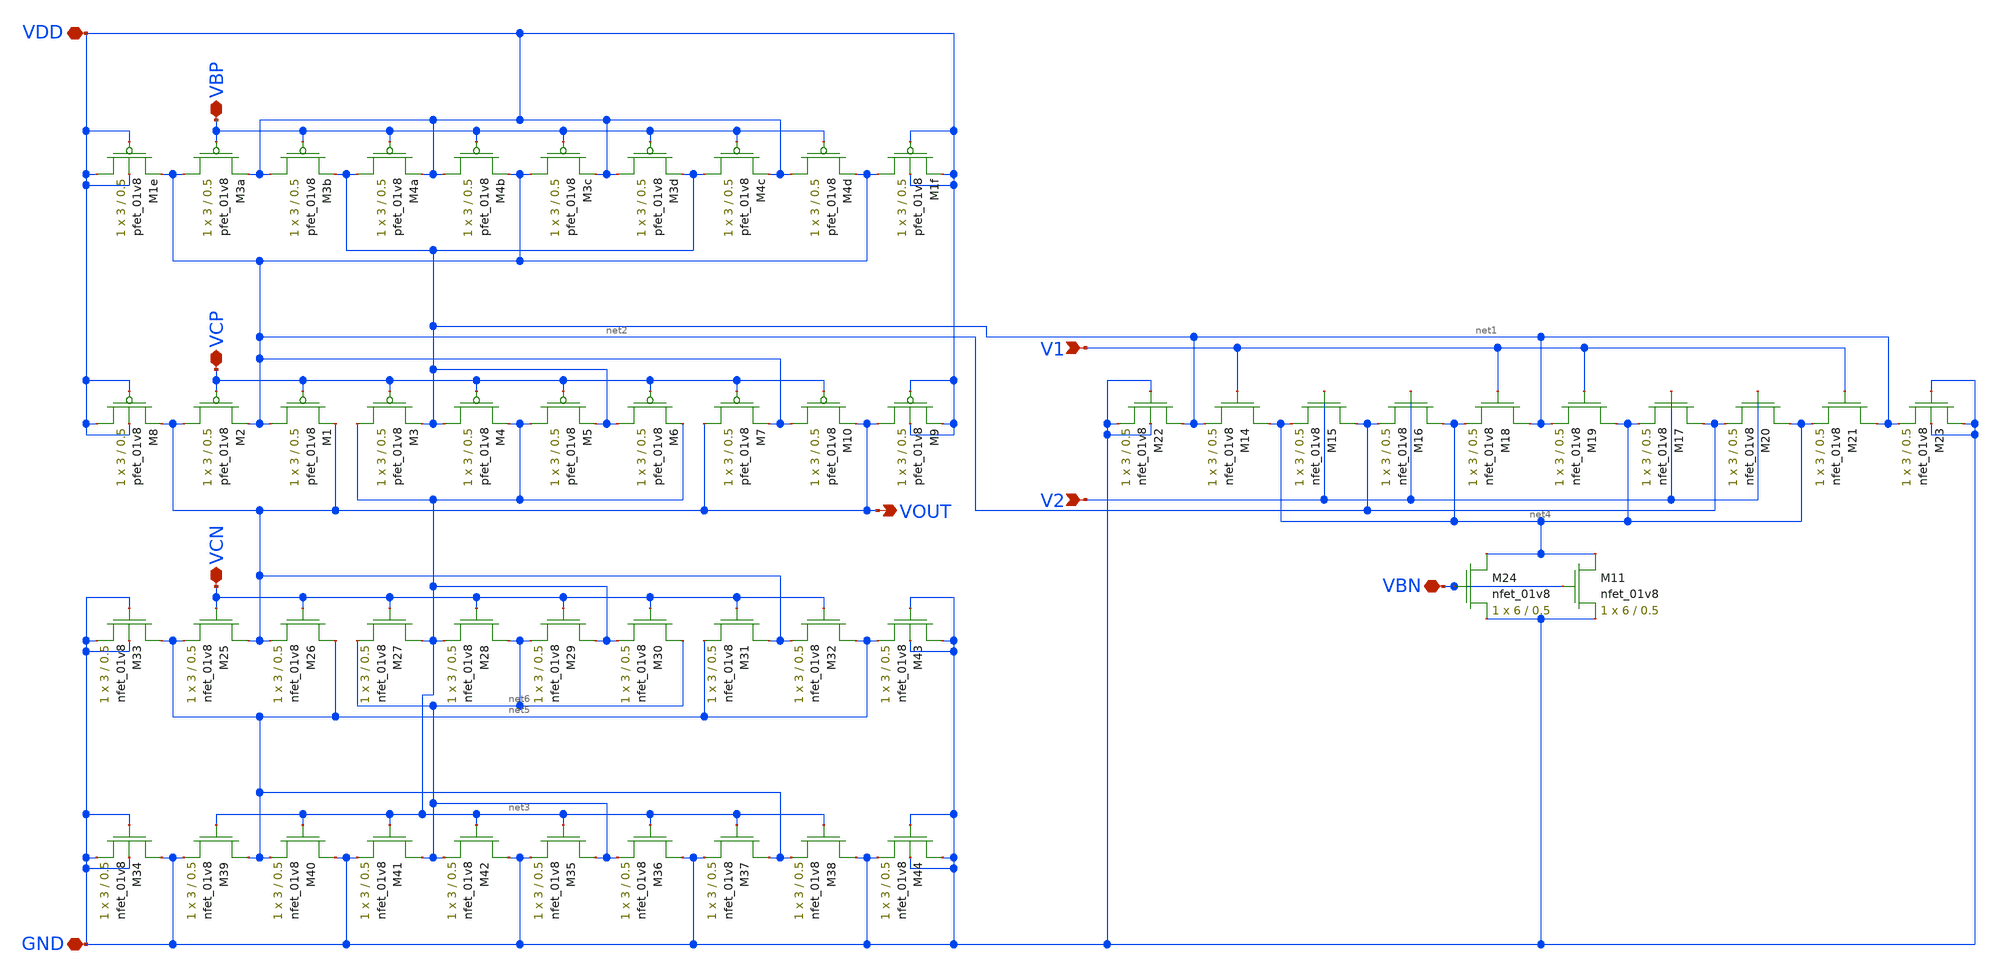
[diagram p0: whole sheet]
** sch_path: mp3/schematics/differential_amplifier.sch
**.subckt differential_amplifier VBP VCP V1 V2 VBN VCN VDD GND VOUT
*.iopin VBP
*.iopin VCP
*.ipin V1
*.ipin V2
*.iopin VBN
*.iopin VCN
*.iopin VDD
*.iopin GND
*.opin VOUT
XM3b VDD VBP net1 VDD sky130_fd_pr__pfet_01v8 L=0.5 W=3 nf=1 ad='int((nf+1)/2) * W/nf * 0.29' as='int((nf+2)/2) * W/nf * 0.29'
+ pd='2*int((nf+1)/2) * (W/nf + 0.29)' ps='2*int((nf+2)/2) * (W/nf + 0.29)' nrd='0.29 / W' nrs='0.29 / W'
+ sa=0 sb=0 sd=0 mult=1 m=1
XM3a net2 VBP VDD VDD sky130_fd_pr__pfet_01v8 L=0.5 W=3 nf=1 ad='int((nf+1)/2) * W/nf * 0.29' as='int((nf+2)/2) * W/nf * 0.29'
+ pd='2*int((nf+1)/2) * (W/nf + 0.29)' ps='2*int((nf+2)/2) * (W/nf + 0.29)' nrd='0.29 / W' nrs='0.29 / W'
+ sa=0 sb=0 sd=0 mult=1 m=1
XM4a net1 VBP VDD VDD sky130_fd_pr__pfet_01v8 L=0.5 W=3 nf=1 ad='int((nf+1)/2) * W/nf * 0.29' as='int((nf+2)/2) * W/nf * 0.29'
+ pd='2*int((nf+1)/2) * (W/nf + 0.29)' ps='2*int((nf+2)/2) * (W/nf + 0.29)' nrd='0.29 / W' nrs='0.29 / W'
+ sa=0 sb=0 sd=0 mult=1 m=1
XM4b VDD VBP net2 VDD sky130_fd_pr__pfet_01v8 L=0.5 W=3 nf=1 ad='int((nf+1)/2) * W/nf * 0.29' as='int((nf+2)/2) * W/nf * 0.29'
+ pd='2*int((nf+1)/2) * (W/nf + 0.29)' ps='2*int((nf+2)/2) * (W/nf + 0.29)' nrd='0.29 / W' nrs='0.29 / W'
+ sa=0 sb=0 sd=0 mult=1 m=1
XM3c net2 VBP VDD VDD sky130_fd_pr__pfet_01v8 L=0.5 W=3 nf=1 ad='int((nf+1)/2) * W/nf * 0.29' as='int((nf+2)/2) * W/nf * 0.29'
+ pd='2*int((nf+1)/2) * (W/nf + 0.29)' ps='2*int((nf+2)/2) * (W/nf + 0.29)' nrd='0.29 / W' nrs='0.29 / W'
+ sa=0 sb=0 sd=0 mult=1 m=1
XM3d VDD VBP net1 VDD sky130_fd_pr__pfet_01v8 L=0.5 W=3 nf=1 ad='int((nf+1)/2) * W/nf * 0.29' as='int((nf+2)/2) * W/nf * 0.29'
+ pd='2*int((nf+1)/2) * (W/nf + 0.29)' ps='2*int((nf+2)/2) * (W/nf + 0.29)' nrd='0.29 / W' nrs='0.29 / W'
+ sa=0 sb=0 sd=0 mult=1 m=1
XM4c net1 VBP VDD VDD sky130_fd_pr__pfet_01v8 L=0.5 W=3 nf=1 ad='int((nf+1)/2) * W/nf * 0.29' as='int((nf+2)/2) * W/nf * 0.29'
+ pd='2*int((nf+1)/2) * (W/nf + 0.29)' ps='2*int((nf+2)/2) * (W/nf + 0.29)' nrd='0.29 / W' nrs='0.29 / W'
+ sa=0 sb=0 sd=0 mult=1 m=1
XM1e VDD VDD net2 VDD sky130_fd_pr__pfet_01v8 L=0.5 W=3 nf=1 ad='int((nf+1)/2) * W/nf * 0.29' as='int((nf+2)/2) * W/nf * 0.29'
+ pd='2*int((nf+1)/2) * (W/nf + 0.29)' ps='2*int((nf+2)/2) * (W/nf + 0.29)' nrd='0.29 / W' nrs='0.29 / W'
+ sa=0 sb=0 sd=0 mult=1 m=1
XM1f net2 VDD VDD VDD sky130_fd_pr__pfet_01v8 L=0.5 W=3 nf=1 ad='int((nf+1)/2) * W/nf * 0.29' as='int((nf+2)/2) * W/nf * 0.29'
+ pd='2*int((nf+1)/2) * (W/nf + 0.29)' ps='2*int((nf+2)/2) * (W/nf + 0.29)' nrd='0.29 / W' nrs='0.29 / W'
+ sa=0 sb=0 sd=0 mult=1 m=1
XM4d VDD VBP net2 VDD sky130_fd_pr__pfet_01v8 L=0.5 W=3 nf=1 ad='int((nf+1)/2) * W/nf * 0.29' as='int((nf+2)/2) * W/nf * 0.29'
+ pd='2*int((nf+1)/2) * (W/nf + 0.29)' ps='2*int((nf+2)/2) * (W/nf + 0.29)' nrd='0.29 / W' nrs='0.29 / W'
+ sa=0 sb=0 sd=0 mult=1 m=1
XM1 net2 VCP VOUT VDD sky130_fd_pr__pfet_01v8 L=0.5 W=3 nf=1 ad='int((nf+1)/2) * W/nf * 0.29' as='int((nf+2)/2) * W/nf * 0.29'
+ pd='2*int((nf+1)/2) * (W/nf + 0.29)' ps='2*int((nf+2)/2) * (W/nf + 0.29)' nrd='0.29 / W' nrs='0.29 / W'
+ sa=0 sb=0 sd=0 mult=1 m=1
XM2 VOUT VCP net2 VDD sky130_fd_pr__pfet_01v8 L=0.5 W=3 nf=1 ad='int((nf+1)/2) * W/nf * 0.29' as='int((nf+2)/2) * W/nf * 0.29'
+ pd='2*int((nf+1)/2) * (W/nf + 0.29)' ps='2*int((nf+2)/2) * (W/nf + 0.29)' nrd='0.29 / W' nrs='0.29 / W'
+ sa=0 sb=0 sd=0 mult=1 m=1
XM3 net3 VCP net1 VDD sky130_fd_pr__pfet_01v8 L=0.5 W=3 nf=1 ad='int((nf+1)/2) * W/nf * 0.29' as='int((nf+2)/2) * W/nf * 0.29'
+ pd='2*int((nf+1)/2) * (W/nf + 0.29)' ps='2*int((nf+2)/2) * (W/nf + 0.29)' nrd='0.29 / W' nrs='0.29 / W'
+ sa=0 sb=0 sd=0 mult=1 m=1
XM4 net1 VCP net3 VDD sky130_fd_pr__pfet_01v8 L=0.5 W=3 nf=1 ad='int((nf+1)/2) * W/nf * 0.29' as='int((nf+2)/2) * W/nf * 0.29'
+ pd='2*int((nf+1)/2) * (W/nf + 0.29)' ps='2*int((nf+2)/2) * (W/nf + 0.29)' nrd='0.29 / W' nrs='0.29 / W'
+ sa=0 sb=0 sd=0 mult=1 m=1
XM5 net3 VCP net1 VDD sky130_fd_pr__pfet_01v8 L=0.5 W=3 nf=1 ad='int((nf+1)/2) * W/nf * 0.29' as='int((nf+2)/2) * W/nf * 0.29'
+ pd='2*int((nf+1)/2) * (W/nf + 0.29)' ps='2*int((nf+2)/2) * (W/nf + 0.29)' nrd='0.29 / W' nrs='0.29 / W'
+ sa=0 sb=0 sd=0 mult=1 m=1
XM6 net1 VCP net3 VDD sky130_fd_pr__pfet_01v8 L=0.5 W=3 nf=1 ad='int((nf+1)/2) * W/nf * 0.29' as='int((nf+2)/2) * W/nf * 0.29'
+ pd='2*int((nf+1)/2) * (W/nf + 0.29)' ps='2*int((nf+2)/2) * (W/nf + 0.29)' nrd='0.29 / W' nrs='0.29 / W'
+ sa=0 sb=0 sd=0 mult=1 m=1
XM7 VOUT VCP net2 VDD sky130_fd_pr__pfet_01v8 L=0.5 W=3 nf=1 ad='int((nf+1)/2) * W/nf * 0.29' as='int((nf+2)/2) * W/nf * 0.29'
+ pd='2*int((nf+1)/2) * (W/nf + 0.29)' ps='2*int((nf+2)/2) * (W/nf + 0.29)' nrd='0.29 / W' nrs='0.29 / W'
+ sa=0 sb=0 sd=0 mult=1 m=1
XM8 VDD VDD VOUT VDD sky130_fd_pr__pfet_01v8 L=0.5 W=3 nf=1 ad='int((nf+1)/2) * W/nf * 0.29' as='int((nf+2)/2) * W/nf * 0.29'
+ pd='2*int((nf+1)/2) * (W/nf + 0.29)' ps='2*int((nf+2)/2) * (W/nf + 0.29)' nrd='0.29 / W' nrs='0.29 / W'
+ sa=0 sb=0 sd=0 mult=1 m=1
XM9 VOUT VDD VDD VDD sky130_fd_pr__pfet_01v8 L=0.5 W=3 nf=1 ad='int((nf+1)/2) * W/nf * 0.29' as='int((nf+2)/2) * W/nf * 0.29'
+ pd='2*int((nf+1)/2) * (W/nf + 0.29)' ps='2*int((nf+2)/2) * (W/nf + 0.29)' nrd='0.29 / W' nrs='0.29 / W'
+ sa=0 sb=0 sd=0 mult=1 m=1
XM10 net2 VCP VOUT VDD sky130_fd_pr__pfet_01v8 L=0.5 W=3 nf=1 ad='int((nf+1)/2) * W/nf * 0.29' as='int((nf+2)/2) * W/nf * 0.29'
+ pd='2*int((nf+1)/2) * (W/nf + 0.29)' ps='2*int((nf+2)/2) * (W/nf + 0.29)' nrd='0.29 / W' nrs='0.29 / W'
+ sa=0 sb=0 sd=0 mult=1 m=1
XM14 net4 V1 net1 GND sky130_fd_pr__nfet_01v8 L=0.5 W=3 nf=1 ad='int((nf+1)/2) * W/nf * 0.29' as='int((nf+2)/2) * W/nf * 0.29'
+ pd='2*int((nf+1)/2) * (W/nf + 0.29)' ps='2*int((nf+2)/2) * (W/nf + 0.29)' nrd='0.29 / W' nrs='0.29 / W'
+ sa=0 sb=0 sd=0 mult=1 m=1
XM22 net1 GND GND GND sky130_fd_pr__nfet_01v8 L=0.5 W=3 nf=1 ad='int((nf+1)/2) * W/nf * 0.29' as='int((nf+2)/2) * W/nf * 0.29'
+ pd='2*int((nf+1)/2) * (W/nf + 0.29)' ps='2*int((nf+2)/2) * (W/nf + 0.29)' nrd='0.29 / W' nrs='0.29 / W'
+ sa=0 sb=0 sd=0 mult=1 m=1
XM23 GND GND net1 GND sky130_fd_pr__nfet_01v8 L=0.5 W=3 nf=1 ad='int((nf+1)/2) * W/nf * 0.29' as='int((nf+2)/2) * W/nf * 0.29'
+ pd='2*int((nf+1)/2) * (W/nf + 0.29)' ps='2*int((nf+2)/2) * (W/nf + 0.29)' nrd='0.29 / W' nrs='0.29 / W'
+ sa=0 sb=0 sd=0 mult=1 m=1
XM15 net2 V2 net4 GND sky130_fd_pr__nfet_01v8 L=0.5 W=3 nf=1 ad='int((nf+1)/2) * W/nf * 0.29' as='int((nf+2)/2) * W/nf * 0.29'
+ pd='2*int((nf+1)/2) * (W/nf + 0.29)' ps='2*int((nf+2)/2) * (W/nf + 0.29)' nrd='0.29 / W' nrs='0.29 / W'
+ sa=0 sb=0 sd=0 mult=1 m=1
XM16 net4 V2 net2 GND sky130_fd_pr__nfet_01v8 L=0.5 W=3 nf=1 ad='int((nf+1)/2) * W/nf * 0.29' as='int((nf+2)/2) * W/nf * 0.29'
+ pd='2*int((nf+1)/2) * (W/nf + 0.29)' ps='2*int((nf+2)/2) * (W/nf + 0.29)' nrd='0.29 / W' nrs='0.29 / W'
+ sa=0 sb=0 sd=0 mult=1 m=1
XM17 net2 V2 net4 GND sky130_fd_pr__nfet_01v8 L=0.5 W=3 nf=1 ad='int((nf+1)/2) * W/nf * 0.29' as='int((nf+2)/2) * W/nf * 0.29'
+ pd='2*int((nf+1)/2) * (W/nf + 0.29)' ps='2*int((nf+2)/2) * (W/nf + 0.29)' nrd='0.29 / W' nrs='0.29 / W'
+ sa=0 sb=0 sd=0 mult=1 m=1
XM18 net1 V1 net4 GND sky130_fd_pr__nfet_01v8 L=0.5 W=3 nf=1 ad='int((nf+1)/2) * W/nf * 0.29' as='int((nf+2)/2) * W/nf * 0.29'
+ pd='2*int((nf+1)/2) * (W/nf + 0.29)' ps='2*int((nf+2)/2) * (W/nf + 0.29)' nrd='0.29 / W' nrs='0.29 / W'
+ sa=0 sb=0 sd=0 mult=1 m=1
XM19 net4 V1 net1 GND sky130_fd_pr__nfet_01v8 L=0.5 W=3 nf=1 ad='int((nf+1)/2) * W/nf * 0.29' as='int((nf+2)/2) * W/nf * 0.29'
+ pd='2*int((nf+1)/2) * (W/nf + 0.29)' ps='2*int((nf+2)/2) * (W/nf + 0.29)' nrd='0.29 / W' nrs='0.29 / W'
+ sa=0 sb=0 sd=0 mult=1 m=1
XM20 net4 V2 net2 GND sky130_fd_pr__nfet_01v8 L=0.5 W=3 nf=1 ad='int((nf+1)/2) * W/nf * 0.29' as='int((nf+2)/2) * W/nf * 0.29'
+ pd='2*int((nf+1)/2) * (W/nf + 0.29)' ps='2*int((nf+2)/2) * (W/nf + 0.29)' nrd='0.29 / W' nrs='0.29 / W'
+ sa=0 sb=0 sd=0 mult=1 m=1
XM21 net1 V1 net4 GND sky130_fd_pr__nfet_01v8 L=0.5 W=3 nf=1 ad='int((nf+1)/2) * W/nf * 0.29' as='int((nf+2)/2) * W/nf * 0.29'
+ pd='2*int((nf+1)/2) * (W/nf + 0.29)' ps='2*int((nf+2)/2) * (W/nf + 0.29)' nrd='0.29 / W' nrs='0.29 / W'
+ sa=0 sb=0 sd=0 mult=1 m=1
XM24 net4 VBN GND GND sky130_fd_pr__nfet_01v8 L=0.5 W=6 nf=1 ad='int((nf+1)/2) * W/nf * 0.29' as='int((nf+2)/2) * W/nf * 0.29'
+ pd='2*int((nf+1)/2) * (W/nf + 0.29)' ps='2*int((nf+2)/2) * (W/nf + 0.29)' nrd='0.29 / W' nrs='0.29 / W'
+ sa=0 sb=0 sd=0 mult=1 m=1
XM29 net3 VCN net6 GND sky130_fd_pr__nfet_01v8 L=0.5 W=3 nf=1 ad='int((nf+1)/2) * W/nf * 0.29' as='int((nf+2)/2) * W/nf * 0.29'
+ pd='2*int((nf+1)/2) * (W/nf + 0.29)' ps='2*int((nf+2)/2) * (W/nf + 0.29)' nrd='0.29 / W' nrs='0.29 / W'
+ sa=0 sb=0 sd=0 mult=1 m=1
XM30 net6 VCN net3 GND sky130_fd_pr__nfet_01v8 L=0.5 W=3 nf=1 ad='int((nf+1)/2) * W/nf * 0.29' as='int((nf+2)/2) * W/nf * 0.29'
+ pd='2*int((nf+1)/2) * (W/nf + 0.29)' ps='2*int((nf+2)/2) * (W/nf + 0.29)' nrd='0.29 / W' nrs='0.29 / W'
+ sa=0 sb=0 sd=0 mult=1 m=1
XM31 VOUT VCN net5 GND sky130_fd_pr__nfet_01v8 L=0.5 W=3 nf=1 ad='int((nf+1)/2) * W/nf * 0.29' as='int((nf+2)/2) * W/nf * 0.29'
+ pd='2*int((nf+1)/2) * (W/nf + 0.29)' ps='2*int((nf+2)/2) * (W/nf + 0.29)' nrd='0.29 / W' nrs='0.29 / W'
+ sa=0 sb=0 sd=0 mult=1 m=1
XM32 net5 VCN VOUT GND sky130_fd_pr__nfet_01v8 L=0.5 W=3 nf=1 ad='int((nf+1)/2) * W/nf * 0.29' as='int((nf+2)/2) * W/nf * 0.29'
+ pd='2*int((nf+1)/2) * (W/nf + 0.29)' ps='2*int((nf+2)/2) * (W/nf + 0.29)' nrd='0.29 / W' nrs='0.29 / W'
+ sa=0 sb=0 sd=0 mult=1 m=1
XM25 VOUT VCN net5 GND sky130_fd_pr__nfet_01v8 L=0.5 W=3 nf=1 ad='int((nf+1)/2) * W/nf * 0.29' as='int((nf+2)/2) * W/nf * 0.29'
+ pd='2*int((nf+1)/2) * (W/nf + 0.29)' ps='2*int((nf+2)/2) * (W/nf + 0.29)' nrd='0.29 / W' nrs='0.29 / W'
+ sa=0 sb=0 sd=0 mult=1 m=1
XM26 net5 VCN VOUT GND sky130_fd_pr__nfet_01v8 L=0.5 W=3 nf=1 ad='int((nf+1)/2) * W/nf * 0.29' as='int((nf+2)/2) * W/nf * 0.29'
+ pd='2*int((nf+1)/2) * (W/nf + 0.29)' ps='2*int((nf+2)/2) * (W/nf + 0.29)' nrd='0.29 / W' nrs='0.29 / W'
+ sa=0 sb=0 sd=0 mult=1 m=1
XM27 net3 VCN net6 GND sky130_fd_pr__nfet_01v8 L=0.5 W=3 nf=1 ad='int((nf+1)/2) * W/nf * 0.29' as='int((nf+2)/2) * W/nf * 0.29'
+ pd='2*int((nf+1)/2) * (W/nf + 0.29)' ps='2*int((nf+2)/2) * (W/nf + 0.29)' nrd='0.29 / W' nrs='0.29 / W'
+ sa=0 sb=0 sd=0 mult=1 m=1
XM28 net6 VCN net3 GND sky130_fd_pr__nfet_01v8 L=0.5 W=3 nf=1 ad='int((nf+1)/2) * W/nf * 0.29' as='int((nf+2)/2) * W/nf * 0.29'
+ pd='2*int((nf+1)/2) * (W/nf + 0.29)' ps='2*int((nf+2)/2) * (W/nf + 0.29)' nrd='0.29 / W' nrs='0.29 / W'
+ sa=0 sb=0 sd=0 mult=1 m=1
XM35 net6 net3 GND GND sky130_fd_pr__nfet_01v8 L=0.5 W=3 nf=1 ad='int((nf+1)/2) * W/nf * 0.29' as='int((nf+2)/2) * W/nf * 0.29'
+ pd='2*int((nf+1)/2) * (W/nf + 0.29)' ps='2*int((nf+2)/2) * (W/nf + 0.29)' nrd='0.29 / W' nrs='0.29 / W'
+ sa=0 sb=0 sd=0 mult=1 m=1
XM36 GND net3 net6 GND sky130_fd_pr__nfet_01v8 L=0.5 W=3 nf=1 ad='int((nf+1)/2) * W/nf * 0.29' as='int((nf+2)/2) * W/nf * 0.29'
+ pd='2*int((nf+1)/2) * (W/nf + 0.29)' ps='2*int((nf+2)/2) * (W/nf + 0.29)' nrd='0.29 / W' nrs='0.29 / W'
+ sa=0 sb=0 sd=0 mult=1 m=1
XM37 net5 net3 GND GND sky130_fd_pr__nfet_01v8 L=0.5 W=3 nf=1 ad='int((nf+1)/2) * W/nf * 0.29' as='int((nf+2)/2) * W/nf * 0.29'
+ pd='2*int((nf+1)/2) * (W/nf + 0.29)' ps='2*int((nf+2)/2) * (W/nf + 0.29)' nrd='0.29 / W' nrs='0.29 / W'
+ sa=0 sb=0 sd=0 mult=1 m=1
XM38 GND net3 net5 GND sky130_fd_pr__nfet_01v8 L=0.5 W=3 nf=1 ad='int((nf+1)/2) * W/nf * 0.29' as='int((nf+2)/2) * W/nf * 0.29'
+ pd='2*int((nf+1)/2) * (W/nf + 0.29)' ps='2*int((nf+2)/2) * (W/nf + 0.29)' nrd='0.29 / W' nrs='0.29 / W'
+ sa=0 sb=0 sd=0 mult=1 m=1
XM39 net5 net3 GND GND sky130_fd_pr__nfet_01v8 L=0.5 W=3 nf=1 ad='int((nf+1)/2) * W/nf * 0.29' as='int((nf+2)/2) * W/nf * 0.29'
+ pd='2*int((nf+1)/2) * (W/nf + 0.29)' ps='2*int((nf+2)/2) * (W/nf + 0.29)' nrd='0.29 / W' nrs='0.29 / W'
+ sa=0 sb=0 sd=0 mult=1 m=1
XM40 GND net3 net5 GND sky130_fd_pr__nfet_01v8 L=0.5 W=3 nf=1 ad='int((nf+1)/2) * W/nf * 0.29' as='int((nf+2)/2) * W/nf * 0.29'
+ pd='2*int((nf+1)/2) * (W/nf + 0.29)' ps='2*int((nf+2)/2) * (W/nf + 0.29)' nrd='0.29 / W' nrs='0.29 / W'
+ sa=0 sb=0 sd=0 mult=1 m=1
XM41 net6 net3 GND GND sky130_fd_pr__nfet_01v8 L=0.5 W=3 nf=1 ad='int((nf+1)/2) * W/nf * 0.29' as='int((nf+2)/2) * W/nf * 0.29'
+ pd='2*int((nf+1)/2) * (W/nf + 0.29)' ps='2*int((nf+2)/2) * (W/nf + 0.29)' nrd='0.29 / W' nrs='0.29 / W'
+ sa=0 sb=0 sd=0 mult=1 m=1
XM42 GND net3 net6 GND sky130_fd_pr__nfet_01v8 L=0.5 W=3 nf=1 ad='int((nf+1)/2) * W/nf * 0.29' as='int((nf+2)/2) * W/nf * 0.29'
+ pd='2*int((nf+1)/2) * (W/nf + 0.29)' ps='2*int((nf+2)/2) * (W/nf + 0.29)' nrd='0.29 / W' nrs='0.29 / W'
+ sa=0 sb=0 sd=0 mult=1 m=1
XM33 net5 GND GND GND sky130_fd_pr__nfet_01v8 L=0.5 W=3 nf=1 ad='int((nf+1)/2) * W/nf * 0.29' as='int((nf+2)/2) * W/nf * 0.29'
+ pd='2*int((nf+1)/2) * (W/nf + 0.29)' ps='2*int((nf+2)/2) * (W/nf + 0.29)' nrd='0.29 / W' nrs='0.29 / W'
+ sa=0 sb=0 sd=0 mult=1 m=1
XM34 GND GND GND GND sky130_fd_pr__nfet_01v8 L=0.5 W=3 nf=1 ad='int((nf+1)/2) * W/nf * 0.29' as='int((nf+2)/2) * W/nf * 0.29'
+ pd='2*int((nf+1)/2) * (W/nf + 0.29)' ps='2*int((nf+2)/2) * (W/nf + 0.29)' nrd='0.29 / W' nrs='0.29 / W'
+ sa=0 sb=0 sd=0 mult=1 m=1
XM43 GND GND net5 GND sky130_fd_pr__nfet_01v8 L=0.5 W=3 nf=1 ad='int((nf+1)/2) * W/nf * 0.29' as='int((nf+2)/2) * W/nf * 0.29'
+ pd='2*int((nf+1)/2) * (W/nf + 0.29)' ps='2*int((nf+2)/2) * (W/nf + 0.29)' nrd='0.29 / W' nrs='0.29 / W'
+ sa=0 sb=0 sd=0 mult=1 m=1
XM44 GND GND GND GND sky130_fd_pr__nfet_01v8 L=0.5 W=3 nf=1 ad='int((nf+1)/2) * W/nf * 0.29' as='int((nf+2)/2) * W/nf * 0.29'
+ pd='2*int((nf+1)/2) * (W/nf + 0.29)' ps='2*int((nf+2)/2) * (W/nf + 0.29)' nrd='0.29 / W' nrs='0.29 / W'
+ sa=0 sb=0 sd=0 mult=1 m=1
XM11 net4 VBN GND GND sky130_fd_pr__nfet_01v8 L=0.5 W=6 nf=1 ad='int((nf+1)/2) * W/nf * 0.29' as='int((nf+2)/2) * W/nf * 0.29'
+ pd='2*int((nf+1)/2) * (W/nf + 0.29)' ps='2*int((nf+2)/2) * (W/nf + 0.29)' nrd='0.29 / W' nrs='0.29 / W'
+ sa=0 sb=0 sd=0 mult=1 m=1
**.ends
.end
